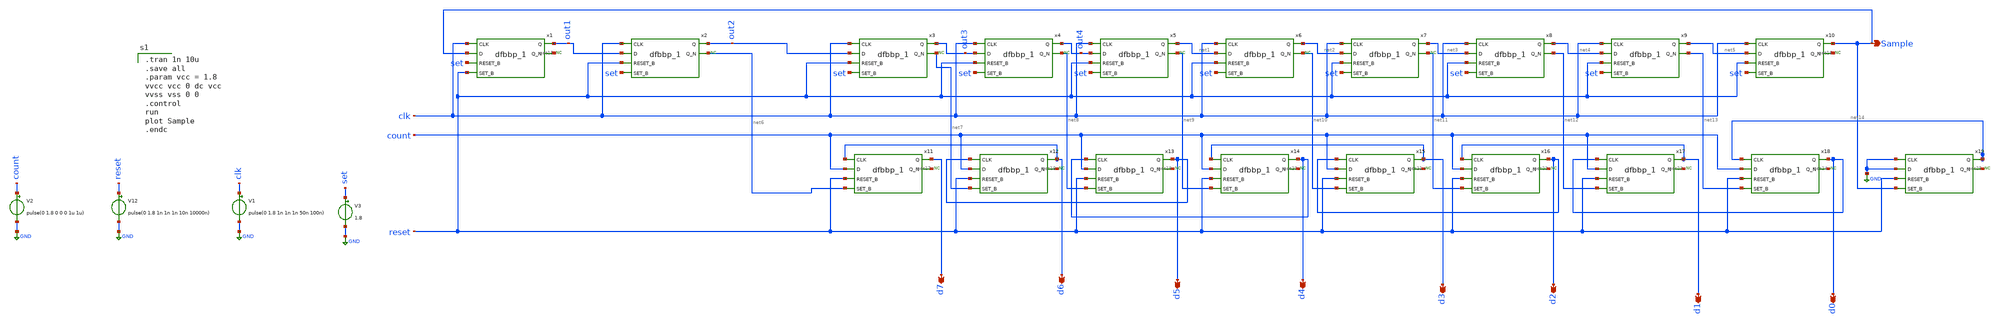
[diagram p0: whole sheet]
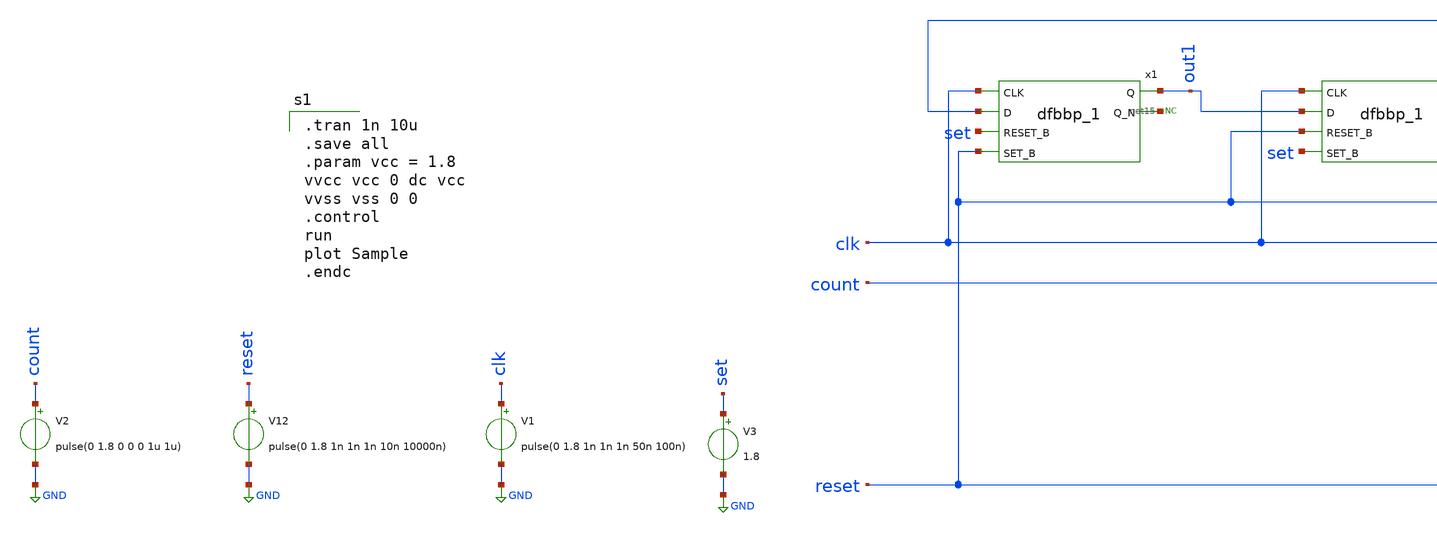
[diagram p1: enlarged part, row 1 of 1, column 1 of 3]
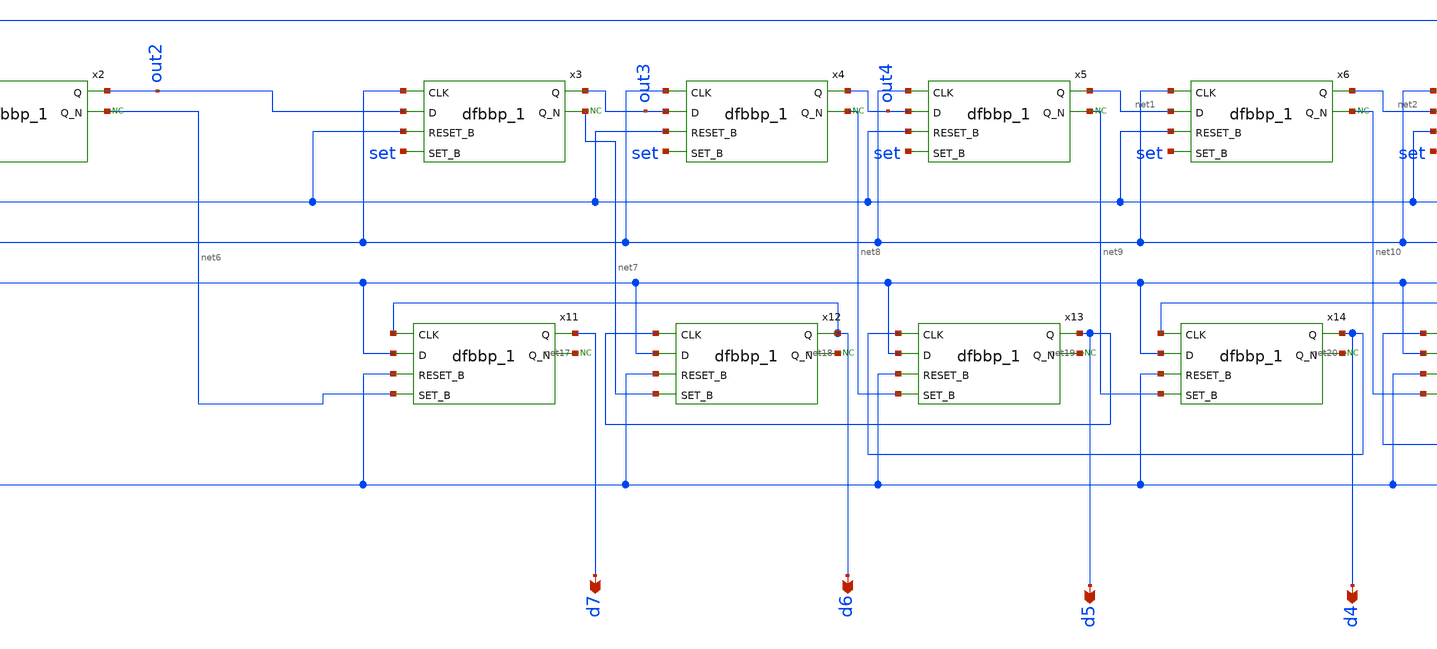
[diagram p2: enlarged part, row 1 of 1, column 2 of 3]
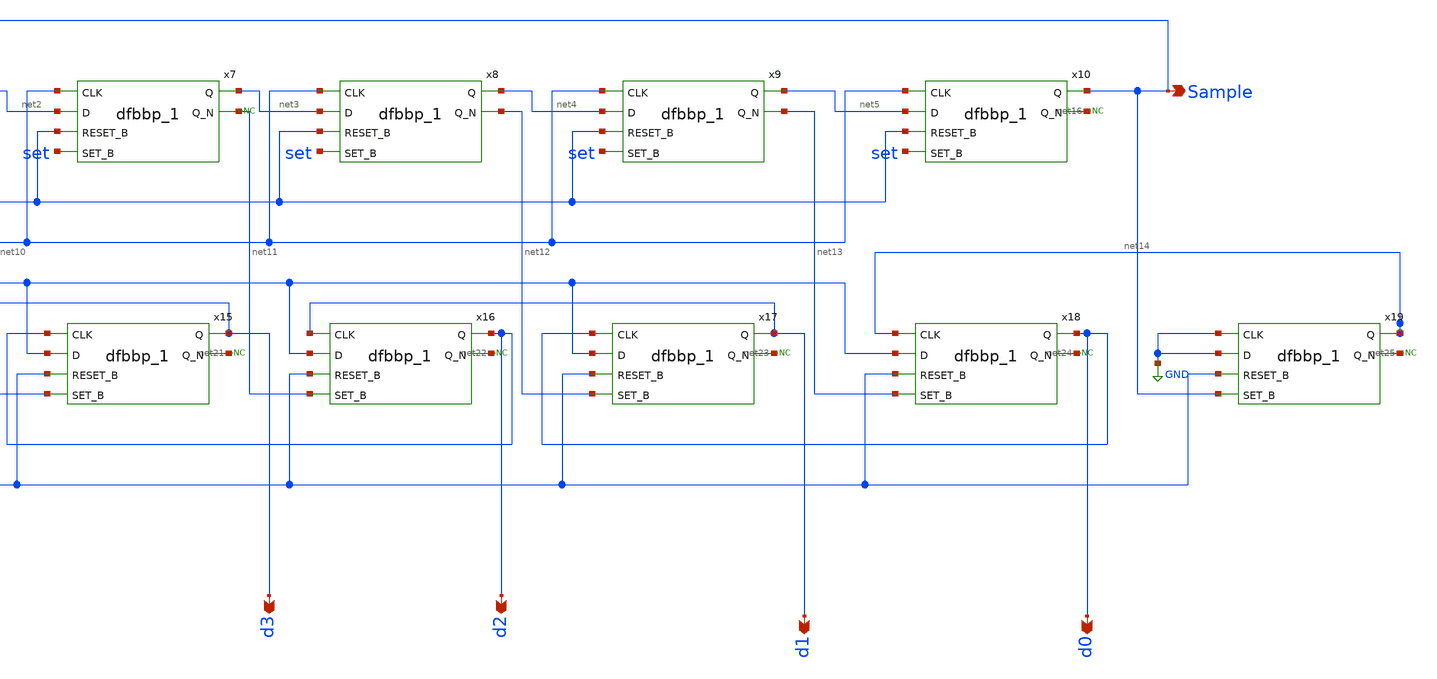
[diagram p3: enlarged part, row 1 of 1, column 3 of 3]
** sch_path: Behavioral_model/controller_tb.sch
* Copyright 2022 Stefan Frederik Schippers
* Licensed under the Apache License, Version 2.0 (the "License");
* you may not use this file except in compliance with the License.
* You may obtain a copy of the License at
* https://www.apache.org/licenses/LICENSE-2.0
* Unless required by applicable law or agreed to in writing, software
* distributed under the License is distributed on an "AS IS" BASIS,
* WITHOUT WARRANTIES OR CONDITIONS OF ANY KIND, either express or implied.
* See the License for the specific language governing permissions and
* limitations under the License.
.lib $::SKYWATER_MODELS/sky130.lib.spice tt
.include $::SKYWATER_STDCELLS/sky130_fd_sc_hd.spice

**.subckt controller_tb d0 d1 d2 d3 d4 d5 d6 d7 Sample
*.opin d0
*.opin d1
*.opin d2
*.opin d3
*.opin d4
*.opin d5
*.opin d6
*.opin d7
*.opin Sample
x1 clk Sample set reset vss vss vcc vcc out1 net15 sky130_fd_sc_hd__dfbbp_1
x2 clk out1 reset set vss vss vcc vcc out2 net6 sky130_fd_sc_hd__dfbbp_1
x3 clk out2 reset set vss vss vcc vcc out3 net7 sky130_fd_sc_hd__dfbbp_1
x4 clk out3 reset set vss vss vcc vcc out4 net8 sky130_fd_sc_hd__dfbbp_1
x5 clk out4 reset set vss vss vcc vcc net1 net9 sky130_fd_sc_hd__dfbbp_1
x6 clk net1 reset set vss vss vcc vcc net2 net10 sky130_fd_sc_hd__dfbbp_1
x7 clk net2 reset set vss vss vcc vcc net3 net11 sky130_fd_sc_hd__dfbbp_1
x8 clk net3 reset set vss vss vcc vcc net4 net12 sky130_fd_sc_hd__dfbbp_1
x9 clk net4 reset set vss vss vcc vcc net5 net13 sky130_fd_sc_hd__dfbbp_1
x10 clk net5 reset set vss vss vcc vcc Sample net16 sky130_fd_sc_hd__dfbbp_1
x11 d6 count reset net6 vss vss vcc vcc d7 net17 sky130_fd_sc_hd__dfbbp_1
x12 d5 count reset net7 vss vss vcc vcc d6 net18 sky130_fd_sc_hd__dfbbp_1
x13 d4 count reset net8 vss vss vcc vcc d5 net19 sky130_fd_sc_hd__dfbbp_1
x14 d3 count reset net9 vss vss vcc vcc d4 net20 sky130_fd_sc_hd__dfbbp_1
x15 d2 count reset net10 vss vss vcc vcc d3 net21 sky130_fd_sc_hd__dfbbp_1
x16 d1 count reset net11 vss vss vcc vcc d2 net22 sky130_fd_sc_hd__dfbbp_1
x17 d0 count reset net12 vss vss vcc vcc d1 net23 sky130_fd_sc_hd__dfbbp_1
x18 net14 count reset net13 vss vss vcc vcc d0 net24 sky130_fd_sc_hd__dfbbp_1
x19 GND GND reset Sample vss vss vcc vcc net14 net25 sky130_fd_sc_hd__dfbbp_1
V12 reset GND pulse(0 1.8 1n 1n 1n 10n 10000n)
V2 count GND pulse(0 1.8 0 0 0 1u 1u)
V3 set GND 1.8
V1 clk GND pulse(0 1.8 1n 1n 1n 50n 100n)
* noconn #net25
* noconn #net24
* noconn #net23
* noconn #net22
* noconn #net21
* noconn #net20
* noconn #net19
* noconn #net18
* noconn #net17
* noconn #net15
* noconn #net6
* noconn #net7
* noconn #net8
* noconn #net9
* noconn #net10
* noconn #net11
* noconn #net16
**** begin user architecture code

.tran 1n 10u
.save all
.param vcc = 1.8
vvcc vcc 0 dc vcc
vvss vss 0 0
.control
run
plot Sample
.endc

**** end user architecture code
**.ends
.GLOBAL GND
.end
